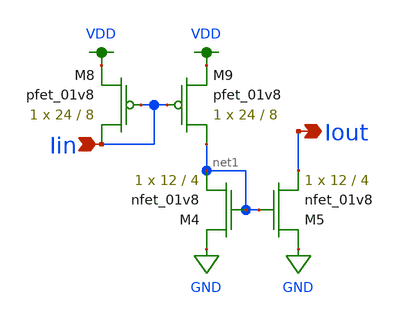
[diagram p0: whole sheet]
** sch_path: modules/simple_mirror_sink.sch
**.subckt simple_mirror_sink Iout Iin
*.opin Iout
*.ipin Iin
XM4 GND net1 net1 GND sky130_fd_pr__nfet_01v8 L=4 W=12 nf=1 ad='int((nf+1)/2) * W/nf * 0.29' as='int((nf+2)/2) * W/nf * 0.29'
+ pd='2*int((nf+1)/2) * (W/nf + 0.29)' ps='2*int((nf+2)/2) * (W/nf + 0.29)' nrd='0.29 / W' nrs='0.29 / W'
+ sa=0 sb=0 sd=0 mult=1 m=1
XM5 GND net1 Iout GND sky130_fd_pr__nfet_01v8 L=4 W=12 nf=1 ad='int((nf+1)/2) * W/nf * 0.29' as='int((nf+2)/2) * W/nf * 0.29'
+ pd='2*int((nf+1)/2) * (W/nf + 0.29)' ps='2*int((nf+2)/2) * (W/nf + 0.29)' nrd='0.29 / W' nrs='0.29 / W'
+ sa=0 sb=0 sd=0 mult=1 m=1
XM8 Iin Iin VDD VDD sky130_fd_pr__pfet_01v8 L=8 W=24 nf=1 ad='int((nf+1)/2) * W/nf * 0.29' as='int((nf+2)/2) * W/nf * 0.29'
+ pd='2*int((nf+1)/2) * (W/nf + 0.29)' ps='2*int((nf+2)/2) * (W/nf + 0.29)' nrd='0.29 / W' nrs='0.29 / W'
+ sa=0 sb=0 sd=0 mult=1 m=1
XM9 net1 Iin VDD VDD sky130_fd_pr__pfet_01v8 L=8 W=24 nf=1 ad='int((nf+1)/2) * W/nf * 0.29' as='int((nf+2)/2) * W/nf * 0.29'
+ pd='2*int((nf+1)/2) * (W/nf + 0.29)' ps='2*int((nf+2)/2) * (W/nf + 0.29)' nrd='0.29 / W' nrs='0.29 / W'
+ sa=0 sb=0 sd=0 mult=1 m=1
**.ends
.GLOBAL GND
.GLOBAL VDD
.end
